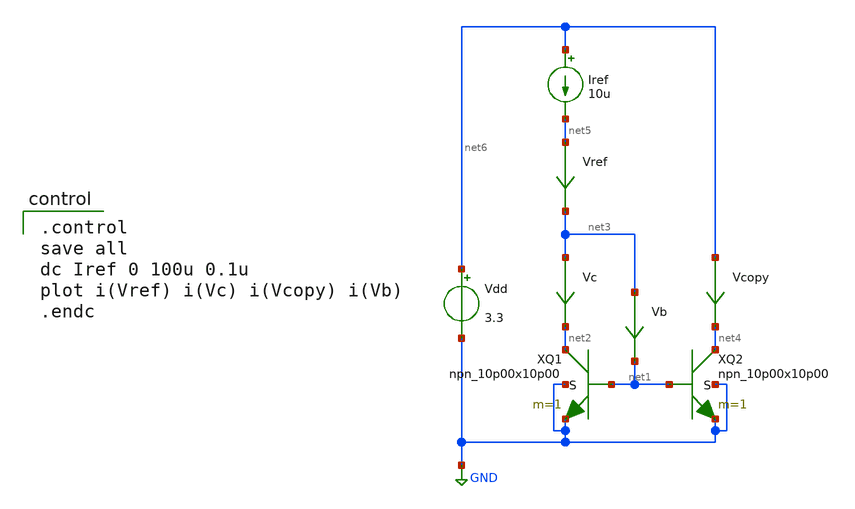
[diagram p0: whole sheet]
** sch_path: bgr/npn-currentmirror_1.sch
**.subckt npn-currentmirror_1
XQ1 net2 net1 GND GND npn_10p00x10p00 m=1
XQ2 net4 net1 GND GND npn_10p00x10p00 m=1
Vdd net6 GND 3.3
Iref net6 net5 10u
Vcopy net6 net4 0
.save i(vcopy)
Vb net3 net1 0
.save i(vb)
Vc net3 net2 0
.save i(vc)
Vref net5 net3 0
.save i(vref)
**** begin user architecture code

.include $::180MCU_MODELS/design.ngspice
.lib $::180MCU_MODELS/sm141064.ngspice typical
.lib $::180MCU_MODELS/sm141064.ngspice res_typical
.lib $::180MCU_MODELS/sm141064.ngspice moscap_typical
.lib $::180MCU_MODELS/sm141064.ngspice bjt_typical
* .lib $::180MCU_MODELS/sm141064.ngspice res_statistical


.control
save all
dc Iref 0 100u 0.1u
plot i(Vref) i(Vc) i(Vcopy) i(Vb)
.endc

**** end user architecture code
**.ends
.GLOBAL GND
.end
